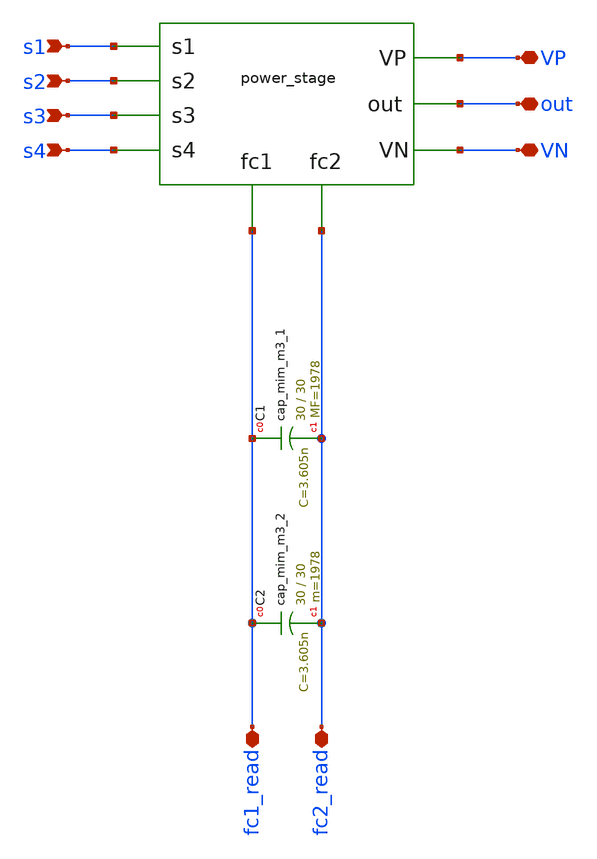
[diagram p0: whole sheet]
** sch_path: DCDC_LDO_sim/converter.sch
**.subckt converter s1 s2 s3 s4 VP VN out fc2_read fc1_read
*.ipin s1
*.ipin s2
*.ipin s3
*.ipin s4
*.iopin VP
*.iopin VN
*.iopin out
*.iopin fc2_read
*.iopin fc1_read
XC1 fc1_read fc2_read sky130_fd_pr__cap_mim_m3_1 W=30 L=30 MF=1978 m=1978
XC2 fc1_read fc2_read sky130_fd_pr__cap_mim_m3_2 W=30 L=30 MF=1978 m=1978
X1 s1 s2 s3 s4 fc1_read fc2_read out VP VN power_stage
**.ends

* expanding   symbol:  /foss/designs/PMIC_lab-on-chip_power-management/DCDC_LDO_sim/power_stage.sym
*+ # of pins=9
** sym_path: DC-DC Converter/Converter/power_stage.sym
** sch_path: DC-DC Converter/Converter/power_stage.sch
.subckt power_stage s1 s2 s3 s4 fc1 fc2 out VP VN
*.iopin VP
*.ipin s1
*.ipin s2
*.iopin out
*.ipin s3
*.ipin s4
*.iopin VN
*.iopin fc1
*.iopin fc2
XM3 out s2 fc1 fc1 sky130_fd_pr__pfet_g5v0d10v5 L=0.5 W=4.38 nf=1 ad='int((nf+1)/2) * W/nf * 0.29' as='int((nf+2)/2) * W/nf * 0.29'
+ pd='2*int((nf+1)/2) * (W/nf + 0.29)' ps='2*int((nf+2)/2) * (W/nf + 0.29)' nrd='0.29 / W' nrs='0.29 / W'
+ sa=0 sb=0 sd=0 mult=4506 m=4506
XM4 fc1 s1 VP VP sky130_fd_pr__pfet_g5v0d10v5 L=0.5 W=4.38 nf=1 ad='int((nf+1)/2) * W/nf * 0.29' as='int((nf+2)/2) * W/nf * 0.29'
+ pd='2*int((nf+1)/2) * (W/nf + 0.29)' ps='2*int((nf+2)/2) * (W/nf + 0.29)' nrd='0.29 / W' nrs='0.29 / W'
+ sa=0 sb=0 sd=0 mult=4506 m=4506
XM1 out s3 fc2 fc2 sky130_fd_pr__nfet_g5v0d10v5 L=0.5 W=4.38 nf=1 ad='int((nf+1)/2) * W/nf * 0.29' as='int((nf+2)/2) * W/nf * 0.29'
+ pd='2*int((nf+1)/2) * (W/nf + 0.29)' ps='2*int((nf+2)/2) * (W/nf + 0.29)' nrd='0.29 / W' nrs='0.29 / W'
+ sa=0 sb=0 sd=0 mult=2520 m=2520
XM2 fc2 s4 VN VN sky130_fd_pr__nfet_g5v0d10v5 L=0.5 W=4.38 nf=1 ad='int((nf+1)/2) * W/nf * 0.29' as='int((nf+2)/2) * W/nf * 0.29'
+ pd='2*int((nf+1)/2) * (W/nf + 0.29)' ps='2*int((nf+2)/2) * (W/nf + 0.29)' nrd='0.29 / W' nrs='0.29 / W'
+ sa=0 sb=0 sd=0 mult=2520 m=2520
.ends

.end
